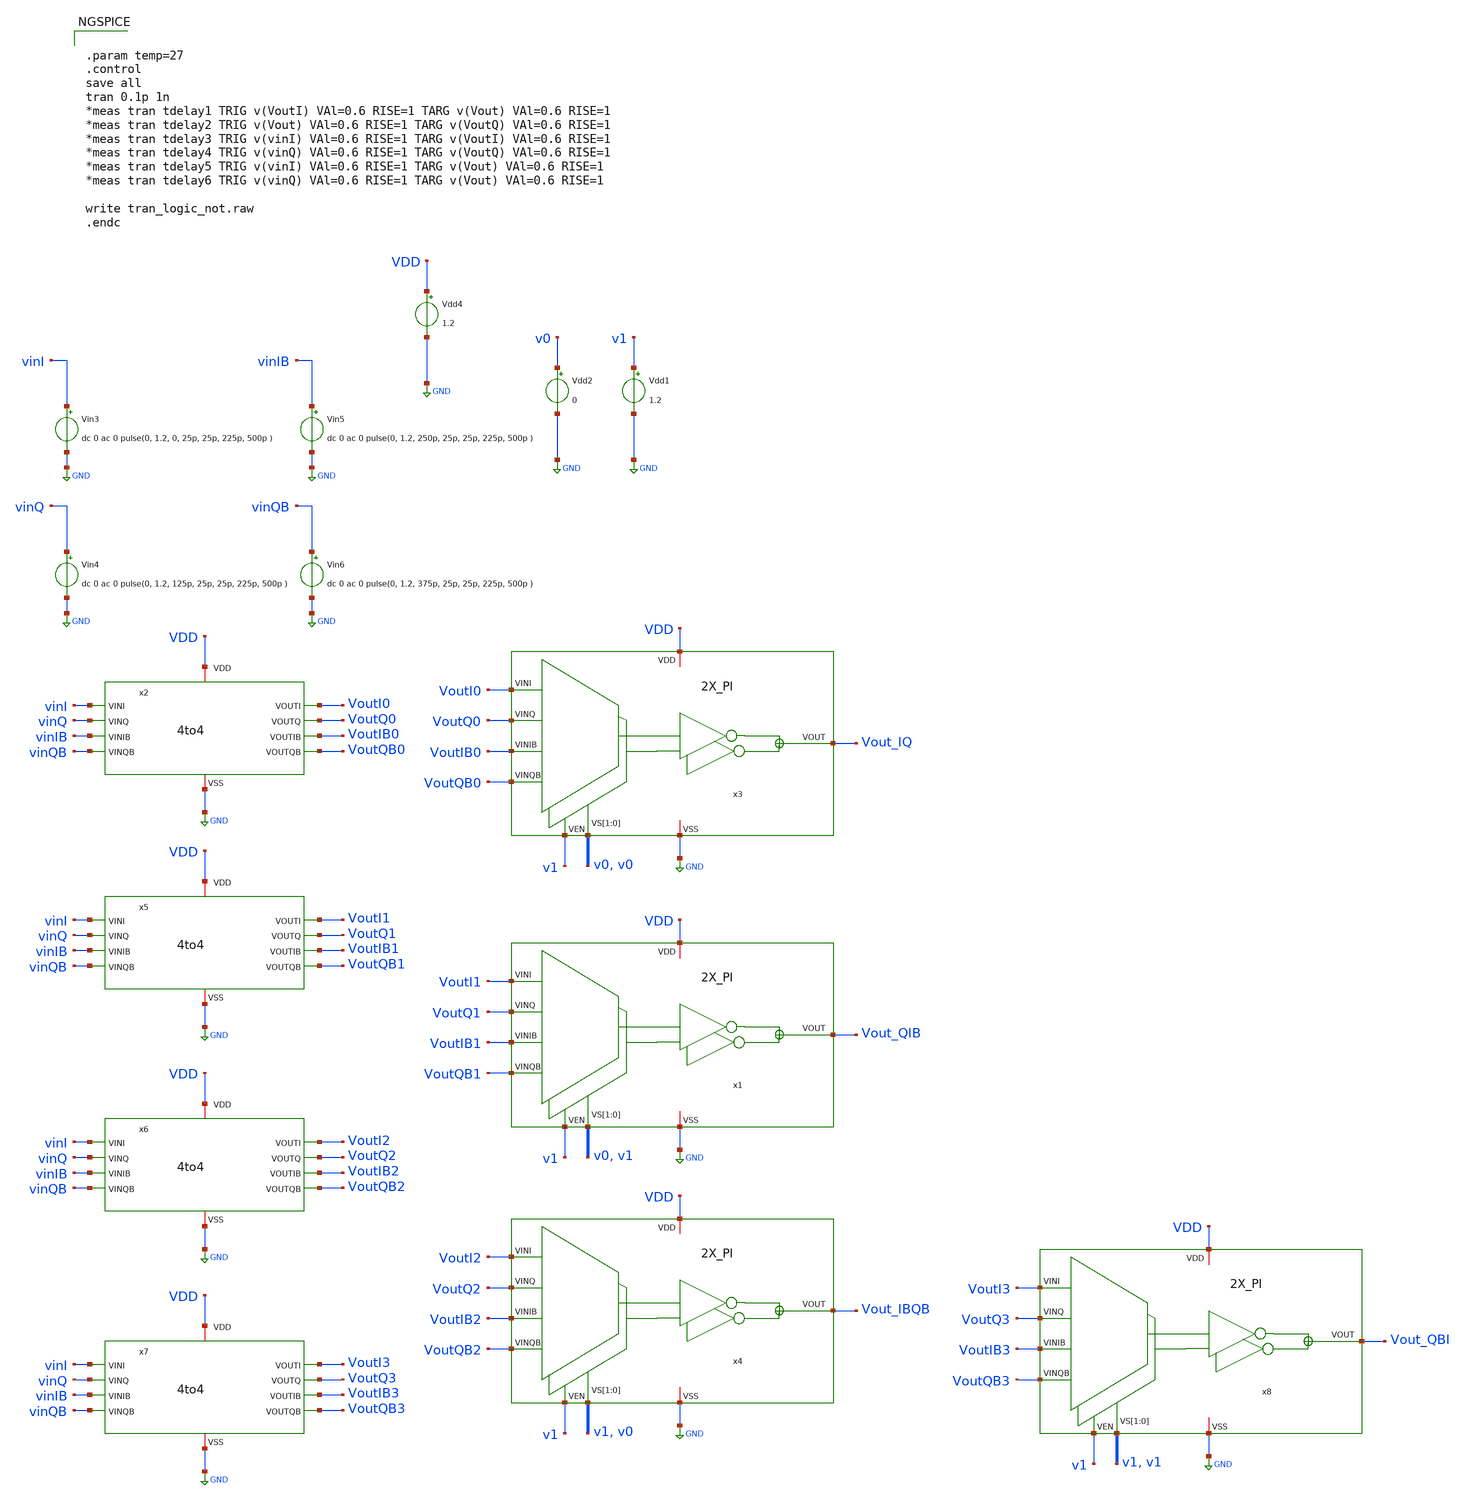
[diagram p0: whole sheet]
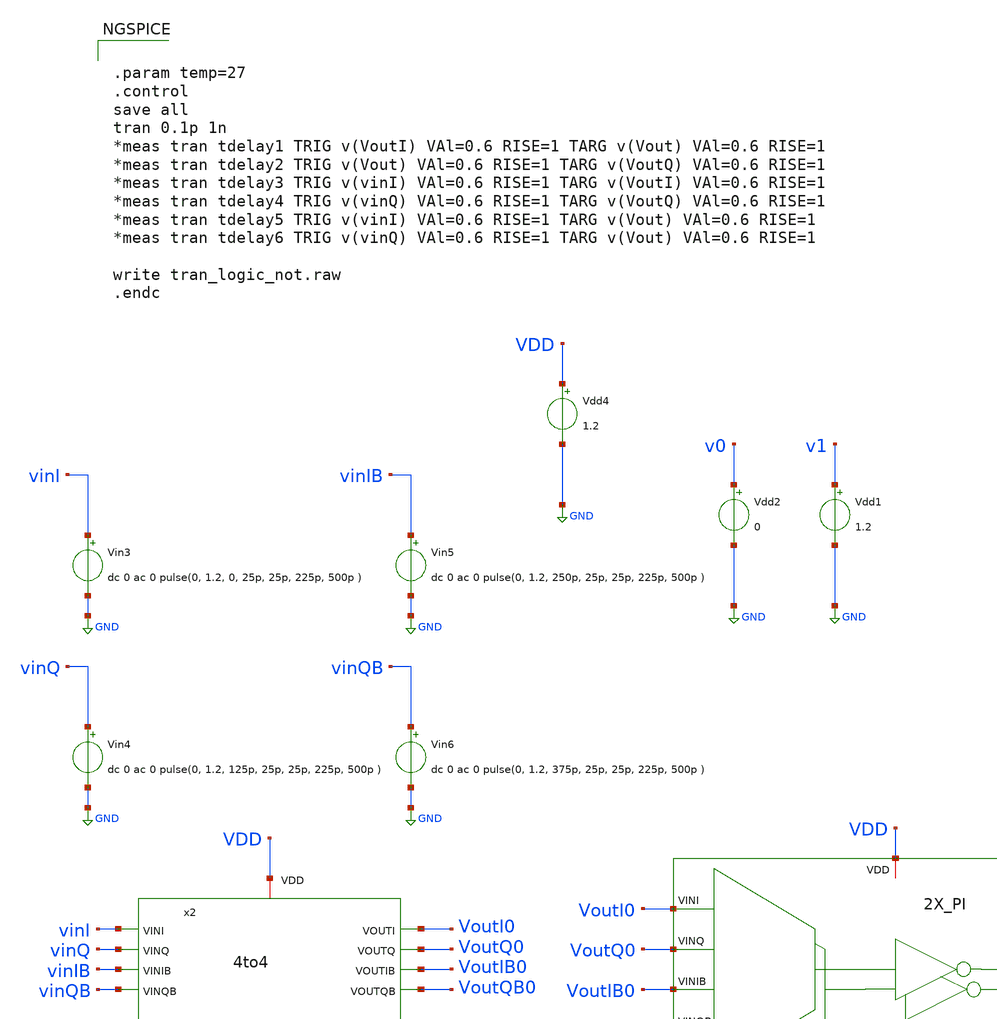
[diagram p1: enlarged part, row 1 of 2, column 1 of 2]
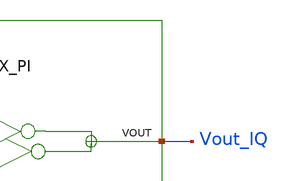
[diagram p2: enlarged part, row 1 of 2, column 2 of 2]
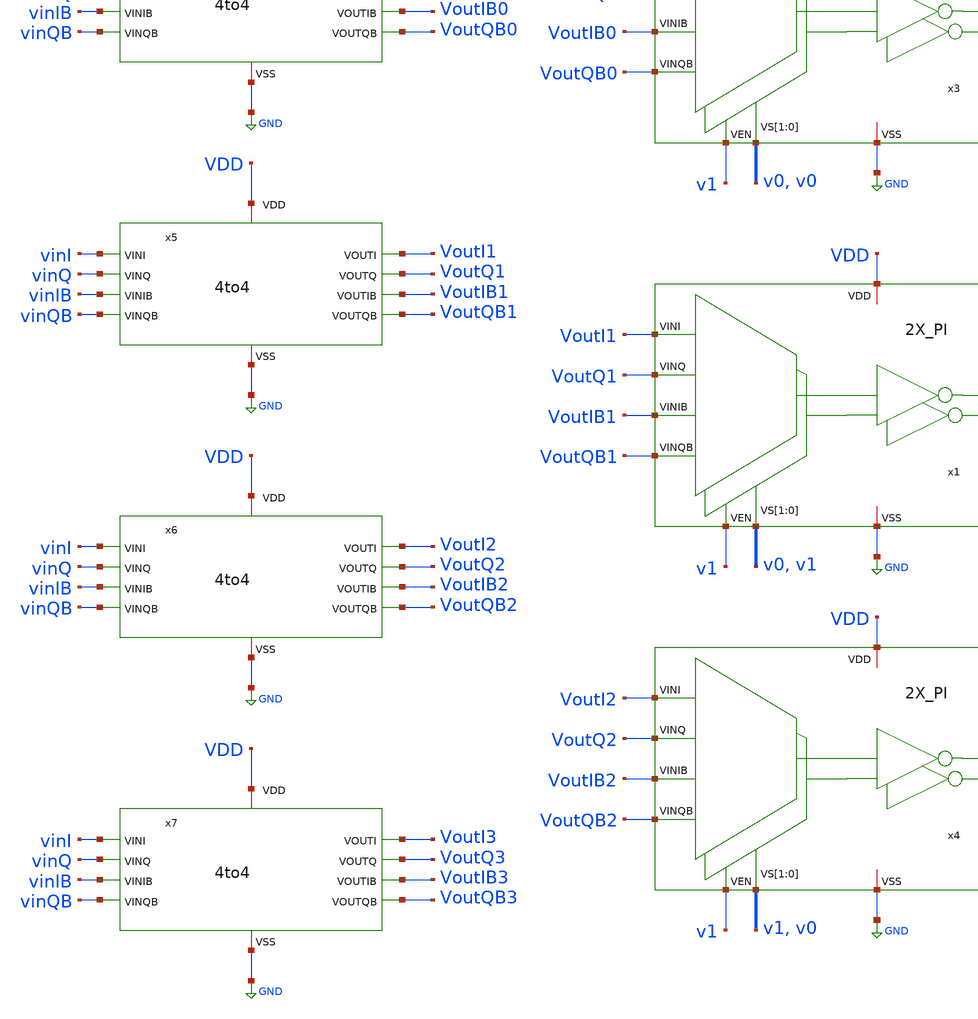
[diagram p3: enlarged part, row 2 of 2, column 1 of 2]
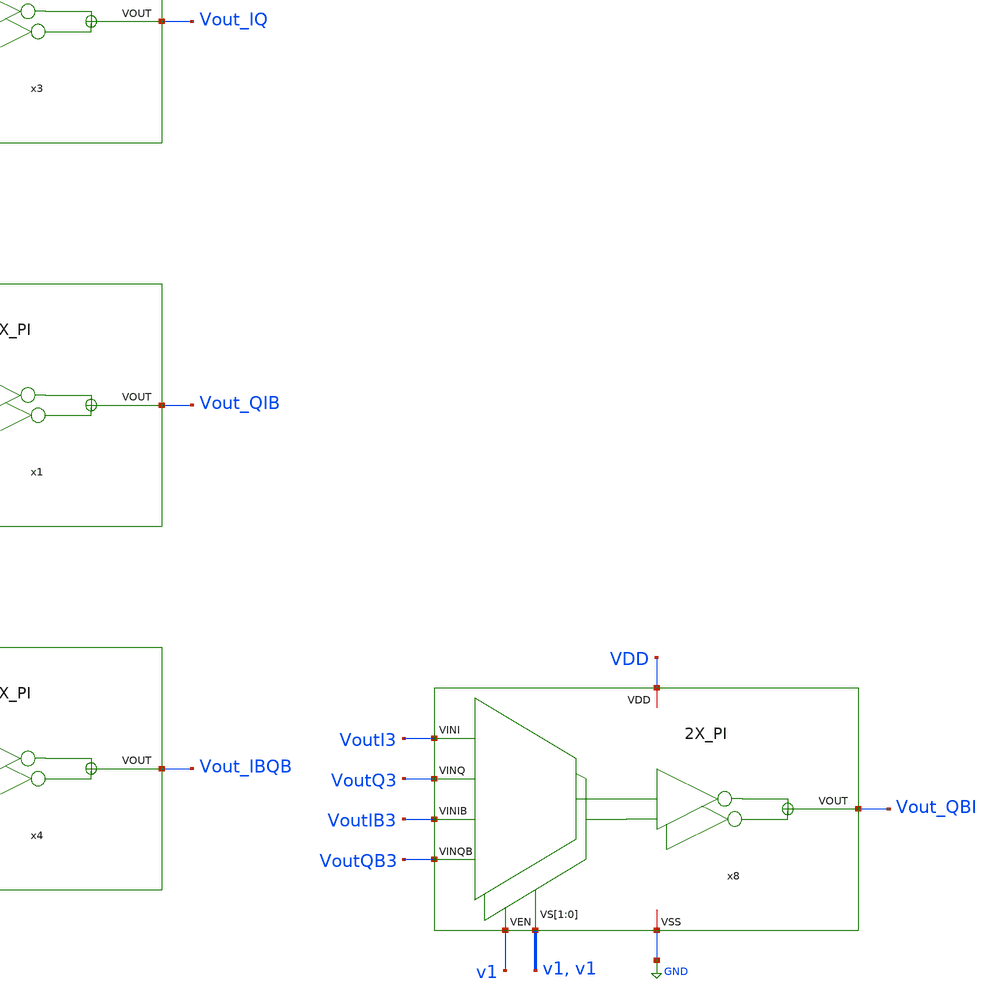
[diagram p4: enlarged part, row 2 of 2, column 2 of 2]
** sch_path: tb_2X_PI_2.sch
**.subckt tb_2X_PI_2
Vdd4 VDD GND 1.2
x1 Vout_QIB v1 VoutI1 VoutQ1 VDD v0 v1 VoutIB1 GND VoutQB1 2X_PI
Vdd1 v1 GND 1.2
Vdd2 v0 GND 0
Vin3 vinI GND dc 0 ac 0 pulse(0, 1.2, 0, 25p, 25p, 225p, 500p )
Vin4 vinQ GND dc 0 ac 0 pulse(0, 1.2, 125p, 25p, 25p, 225p, 500p )
Vin5 vinIB GND dc 0 ac 0 pulse(0, 1.2, 250p, 25p, 25p, 225p, 500p )
Vin6 vinQB GND dc 0 ac 0 pulse(0, 1.2, 375p, 25p, 25p, 225p, 500p )
x2 VDD vinI VoutI0 VoutQ0 vinQ vinIB VoutIB0 vinQB VoutQB0 GND 4to4
x3 Vout_IQ v1 VoutI0 VoutQ0 VDD v0 v0 VoutIB0 GND VoutQB0 2X_PI
x4 Vout_IBQB v1 VoutI2 VoutQ2 VDD v1 v0 VoutIB2 GND VoutQB2 2X_PI
x5 VDD vinI VoutI1 VoutQ1 vinQ vinIB VoutIB1 vinQB VoutQB1 GND 4to4
x6 VDD vinI VoutI2 VoutQ2 vinQ vinIB VoutIB2 vinQB VoutQB2 GND 4to4
x7 VDD vinI VoutI3 VoutQ3 vinQ vinIB VoutIB3 vinQB VoutQB3 GND 4to4
x8 Vout_QBI v1 VoutI3 VoutQ3 VDD v1 v1 VoutIB3 GND VoutQB3 2X_PI
**** begin user architecture code


.param temp=27
.control
save all
tran 0.1p 1n
*meas tran tdelay1 TRIG v(VoutI) VAl=0.6 RISE=1 TARG v(Vout) VAl=0.6 RISE=1
*meas tran tdelay2 TRIG v(Vout) VAl=0.6 RISE=1 TARG v(VoutQ) VAl=0.6 RISE=1
*meas tran tdelay3 TRIG v(vinI) VAl=0.6 RISE=1 TARG v(VoutI) VAl=0.6 RISE=1
*meas tran tdelay4 TRIG v(vinQ) VAl=0.6 RISE=1 TARG v(VoutQ) VAl=0.6 RISE=1
*meas tran tdelay5 TRIG v(vinI) VAl=0.6 RISE=1 TARG v(Vout) VAl=0.6 RISE=1
*meas tran tdelay6 TRIG v(vinQ) VAl=0.6 RISE=1 TARG v(Vout) VAl=0.6 RISE=1

write tran_logic_not.raw
.endc



.lib cornerMOSlv.lib mos_tt

**** end user architecture code
**.ends
.GLOBAL GND
.end
